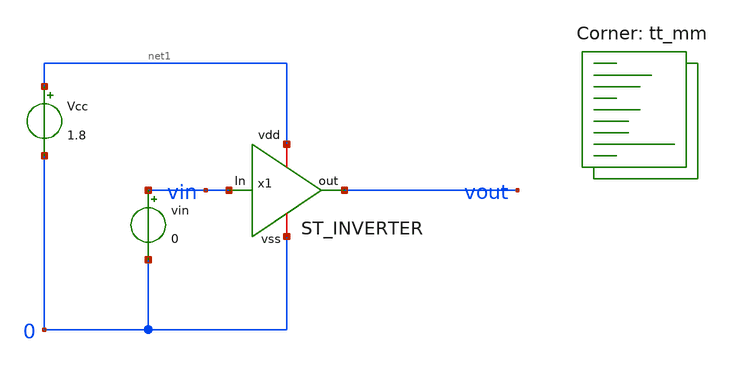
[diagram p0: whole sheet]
** sch_path: Testbenches/ST_INVERTER_TB/schematic/ST_INVERTER_TB.sch
**.subckt ST_INVERTER_TB
Vcc net1 0 1.8
vin vin 0 0
x1 net1 vin vout 0 ST_INVERTER
**** begin user architecture code
.lib $::SKYWATER_MODELS/sky130.lib.spice tt_mm
**** end user architecture code
**.ends

* expanding   symbol:  Component_Library/ST_INVERTER/schematic/ST_INVERTER.sym # of pins=4
** sym_path: Component_Library/ST_INVERTER/schematic/ST_INVERTER.sym
** sch_path: Component_Library/ST_INVERTER/schematic/ST_INVERTER.sch
.subckt ST_INVERTER vdd In out vss
*.ipin In
*.opin out
*.iopin vdd
*.iopin vss
XM2 out In net2 net2 sky130_fd_pr__pfet_01v8 L=0.15 W=1 nf=1 ad='int((nf+1)/2) * W/nf * 0.29' as='int((nf+2)/2) * W/nf * 0.29'
+ pd='2*int((nf+1)/2) * (W/nf + 0.29)' ps='2*int((nf+2)/2) * (W/nf + 0.29)' nrd='0.29 / W' nrs='0.29 / W'
+ sa=0 sb=0 sd=0 mult=1 m=1
XM3 vss out net2 net2 sky130_fd_pr__pfet_01v8 L=0.15 W=1 nf=1 ad='int((nf+1)/2) * W/nf * 0.29' as='int((nf+2)/2) * W/nf * 0.29'
+ pd='2*int((nf+1)/2) * (W/nf + 0.29)' ps='2*int((nf+2)/2) * (W/nf + 0.29)' nrd='0.29 / W' nrs='0.29 / W'
+ sa=0 sb=0 sd=0 mult=1 m=1
XM1 net2 In vdd vdd sky130_fd_pr__pfet_01v8 L=0.15 W=1 nf=1 ad='int((nf+1)/2) * W/nf * 0.29' as='int((nf+2)/2) * W/nf * 0.29'
+ pd='2*int((nf+1)/2) * (W/nf + 0.29)' ps='2*int((nf+2)/2) * (W/nf + 0.29)' nrd='0.29 / W' nrs='0.29 / W'
+ sa=0 sb=0 sd=0 mult=1 m=1
XM4 out In net1 net1 sky130_fd_pr__nfet_01v8 L=0.15 W=1 nf=1 ad='int((nf+1)/2) * W/nf * 0.29' as='int((nf+2)/2) * W/nf * 0.29'
+ pd='2*int((nf+1)/2) * (W/nf + 0.29)' ps='2*int((nf+2)/2) * (W/nf + 0.29)' nrd='0.29 / W' nrs='0.29 / W'
+ sa=0 sb=0 sd=0 mult=1 m=1
XM5 net1 In vss vss sky130_fd_pr__nfet_01v8 L=0.15 W=1 nf=1 ad='int((nf+1)/2) * W/nf * 0.29' as='int((nf+2)/2) * W/nf * 0.29'
+ pd='2*int((nf+1)/2) * (W/nf + 0.29)' ps='2*int((nf+2)/2) * (W/nf + 0.29)' nrd='0.29 / W' nrs='0.29 / W'
+ sa=0 sb=0 sd=0 mult=1 m=1
XM6 vdd out net1 net1 sky130_fd_pr__nfet_01v8 L=0.15 W=1 nf=1 ad='int((nf+1)/2) * W/nf * 0.29' as='int((nf+2)/2) * W/nf * 0.29'
+ pd='2*int((nf+1)/2) * (W/nf + 0.29)' ps='2*int((nf+2)/2) * (W/nf + 0.29)' nrd='0.29 / W' nrs='0.29 / W'
+ sa=0 sb=0 sd=0 mult=1 m=1
.ends

**** begin user architecture code



.option temp = 27

*write ST_INVERTER_TB.raw

.control
*  option seed = 8
  let run = 1
  set filetype=ascii
  save all
  reset
  set appendwrite
  dowhile run < = 1
	dc vin 0 1.8 0.001
	save all
	write ST_INVERTER_TB.raw
	let run=run + 1
	reset
   end
.endc



**** end user architecture code
.end
